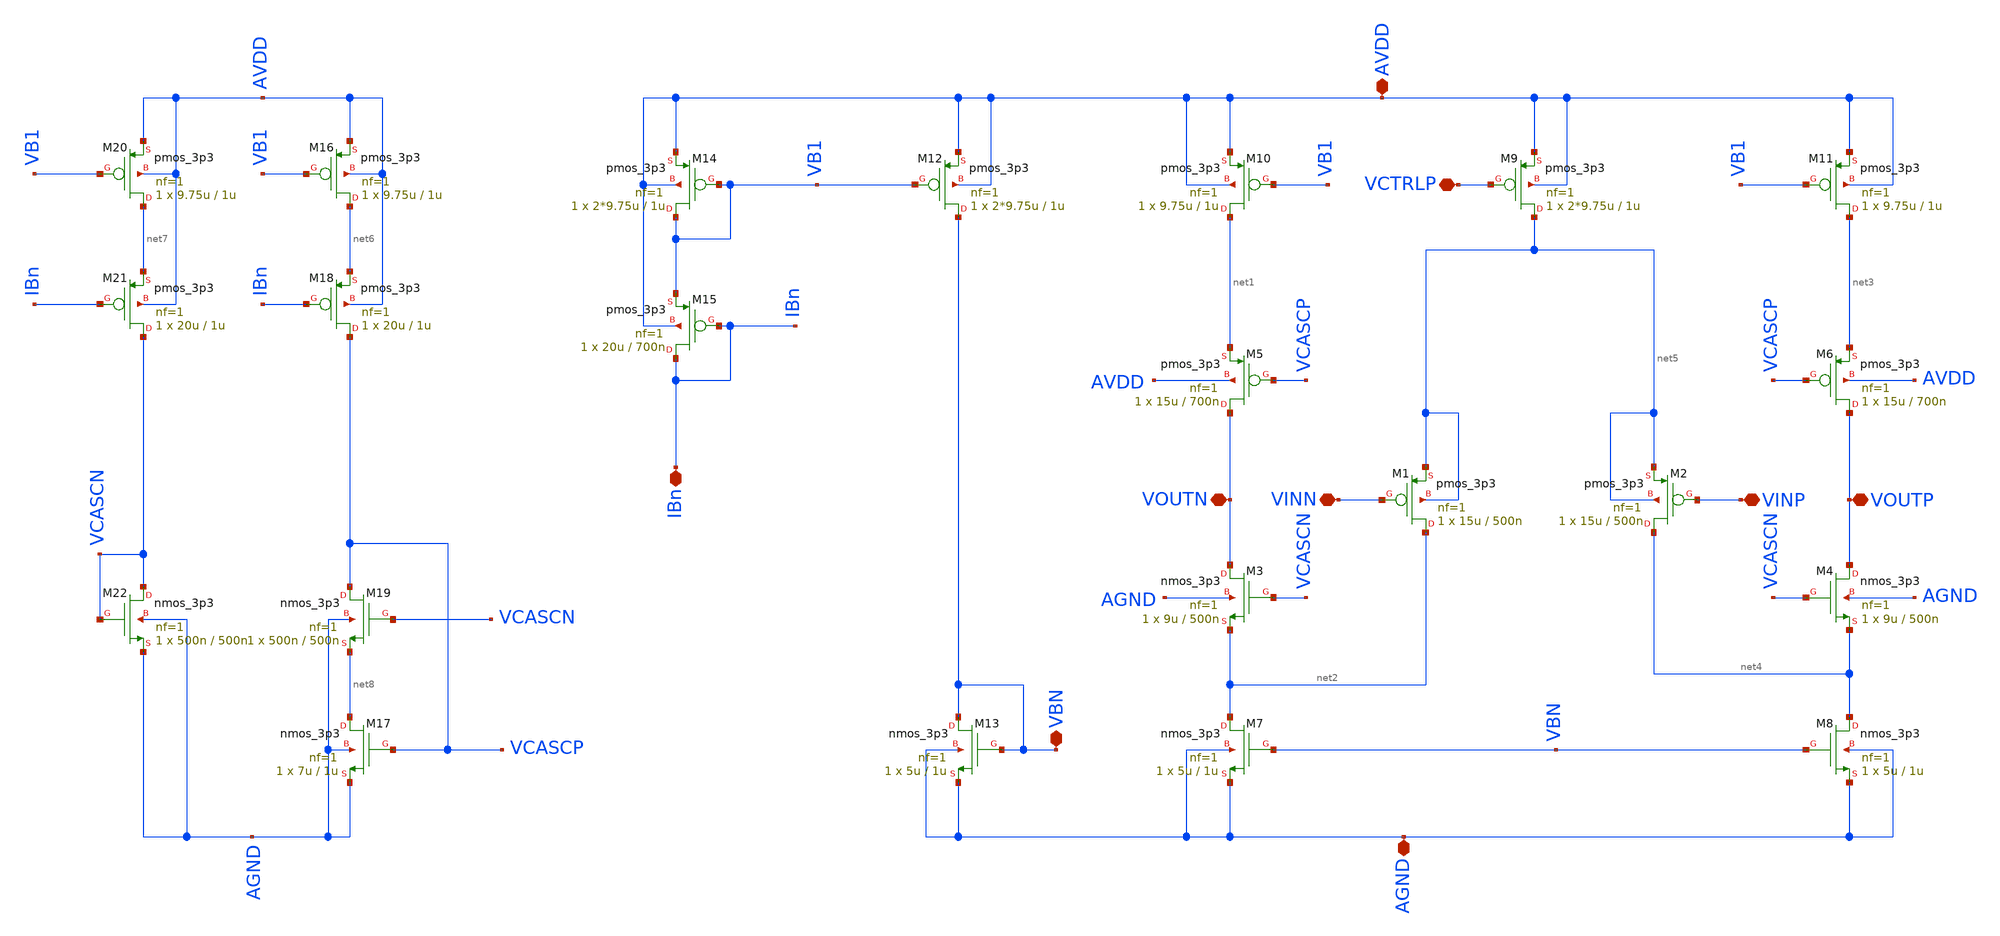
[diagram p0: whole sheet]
** sch_path: ITI_Labs/Lab11_Xschem/Design/OTA copy.sch
**.subckt OTA copy IBn AVDD AGND VINN VINP VOUTN VOUTP VCTRLP VBN
*.iopin IBn
*.iopin AVDD
*.iopin AGND
*.iopin VINN
*.iopin VINP
*.iopin VOUTN
*.iopin VOUTP
*.iopin VCTRLP
*.iopin VBN
XM2 net4 VINP net5 net5 pmos_3p3 L=500n W=15u nf=1 ad='int((nf+1)/2) * W/nf * 0.18u' as='int((nf+2)/2) * W/nf * 0.18u'
+ pd='2*int((nf+1)/2) * (W/nf + 0.18u)' ps='2*int((nf+2)/2) * (W/nf + 0.18u)' nrd='0.18u / W' nrs='0.18u / W'
+ sa=0 sb=0 sd=0 m=1
XM1 net2 VINN net5 net5 pmos_3p3 L=500n W=15u nf=1 ad='int((nf+1)/2) * W/nf * 0.18u' as='int((nf+2)/2) * W/nf * 0.18u'
+ pd='2*int((nf+1)/2) * (W/nf + 0.18u)' ps='2*int((nf+2)/2) * (W/nf + 0.18u)' nrd='0.18u / W' nrs='0.18u / W'
+ sa=0 sb=0 sd=0 m=1
XM9 net5 VCTRLP AVDD AVDD pmos_3p3 L=1u W=2*9.75u nf=1 ad='int((nf+1)/2) * W/nf * 0.18u' as='int((nf+2)/2) * W/nf * 0.18u'
+ pd='2*int((nf+1)/2) * (W/nf + 0.18u)' ps='2*int((nf+2)/2) * (W/nf + 0.18u)' nrd='0.18u / W' nrs='0.18u / W'
+ sa=0 sb=0 sd=0 m=1
XM6 VOUTP VCASCP net3 AVDD pmos_3p3 L=700n W=15u nf=1 ad='int((nf+1)/2) * W/nf * 0.18u' as='int((nf+2)/2) * W/nf * 0.18u'
+ pd='2*int((nf+1)/2) * (W/nf + 0.18u)' ps='2*int((nf+2)/2) * (W/nf + 0.18u)' nrd='0.18u / W' nrs='0.18u / W'
+ sa=0 sb=0 sd=0 m=1
XM11 net3 VB1 AVDD AVDD pmos_3p3 L=1u W=9.75u nf=1 ad='int((nf+1)/2) * W/nf * 0.18u' as='int((nf+2)/2) * W/nf * 0.18u'
+ pd='2*int((nf+1)/2) * (W/nf + 0.18u)' ps='2*int((nf+2)/2) * (W/nf + 0.18u)' nrd='0.18u / W' nrs='0.18u / W'
+ sa=0 sb=0 sd=0 m=1
XM4 VOUTP VCASCN net4 AGND nmos_3p3 L=500n W=9u nf=1 ad='int((nf+1)/2) * W/nf * 0.18u' as='int((nf+2)/2) * W/nf * 0.18u'
+ pd='2*int((nf+1)/2) * (W/nf + 0.18u)' ps='2*int((nf+2)/2) * (W/nf + 0.18u)' nrd='0.18u / W' nrs='0.18u / W'
+ sa=0 sb=0 sd=0 m=1
XM8 net4 VBN AGND AGND nmos_3p3 L=1u W=5u nf=1 ad='int((nf+1)/2) * W/nf * 0.18u' as='int((nf+2)/2) * W/nf * 0.18u'
+ pd='2*int((nf+1)/2) * (W/nf + 0.18u)' ps='2*int((nf+2)/2) * (W/nf + 0.18u)' nrd='0.18u / W' nrs='0.18u / W'
+ sa=0 sb=0 sd=0 m=1
XM5 VOUTN VCASCP net1 AVDD pmos_3p3 L=700n W=15u nf=1 ad='int((nf+1)/2) * W/nf * 0.18u' as='int((nf+2)/2) * W/nf * 0.18u'
+ pd='2*int((nf+1)/2) * (W/nf + 0.18u)' ps='2*int((nf+2)/2) * (W/nf + 0.18u)' nrd='0.18u / W' nrs='0.18u / W'
+ sa=0 sb=0 sd=0 m=1
XM10 net1 VB1 AVDD AVDD pmos_3p3 L=1u W=9.75u nf=1 ad='int((nf+1)/2) * W/nf * 0.18u' as='int((nf+2)/2) * W/nf * 0.18u'
+ pd='2*int((nf+1)/2) * (W/nf + 0.18u)' ps='2*int((nf+2)/2) * (W/nf + 0.18u)' nrd='0.18u / W' nrs='0.18u / W'
+ sa=0 sb=0 sd=0 m=1
XM3 VOUTN VCASCN net2 AGND nmos_3p3 L=500n W=9u nf=1 ad='int((nf+1)/2) * W/nf * 0.18u' as='int((nf+2)/2) * W/nf * 0.18u'
+ pd='2*int((nf+1)/2) * (W/nf + 0.18u)' ps='2*int((nf+2)/2) * (W/nf + 0.18u)' nrd='0.18u / W' nrs='0.18u / W'
+ sa=0 sb=0 sd=0 m=1
XM7 net2 VBN AGND AGND nmos_3p3 L=1u W=5u nf=1 ad='int((nf+1)/2) * W/nf * 0.18u' as='int((nf+2)/2) * W/nf * 0.18u'
+ pd='2*int((nf+1)/2) * (W/nf + 0.18u)' ps='2*int((nf+2)/2) * (W/nf + 0.18u)' nrd='0.18u / W' nrs='0.18u / W'
+ sa=0 sb=0 sd=0 m=1
XM12 VBN VB1 AVDD AVDD pmos_3p3 L=1u W=2*9.75u nf=1 ad='int((nf+1)/2) * W/nf * 0.18u' as='int((nf+2)/2) * W/nf * 0.18u'
+ pd='2*int((nf+1)/2) * (W/nf + 0.18u)' ps='2*int((nf+2)/2) * (W/nf + 0.18u)' nrd='0.18u / W' nrs='0.18u / W'
+ sa=0 sb=0 sd=0 m=1
XM13 VBN VBN AGND AGND nmos_3p3 L=1u W=5u nf=1 ad='int((nf+1)/2) * W/nf * 0.18u' as='int((nf+2)/2) * W/nf * 0.18u'
+ pd='2*int((nf+1)/2) * (W/nf + 0.18u)' ps='2*int((nf+2)/2) * (W/nf + 0.18u)' nrd='0.18u / W' nrs='0.18u / W'
+ sa=0 sb=0 sd=0 m=1
XM14 VB1 VB1 AVDD AVDD pmos_3p3 L=1u W=2*9.75u nf=1 ad='int((nf+1)/2) * W/nf * 0.18u' as='int((nf+2)/2) * W/nf * 0.18u'
+ pd='2*int((nf+1)/2) * (W/nf + 0.18u)' ps='2*int((nf+2)/2) * (W/nf + 0.18u)' nrd='0.18u / W' nrs='0.18u / W'
+ sa=0 sb=0 sd=0 m=1
XM15 IBn IBn VB1 AVDD pmos_3p3 L=700n W=20u nf=1 ad='int((nf+1)/2) * W/nf * 0.18u' as='int((nf+2)/2) * W/nf * 0.18u'
+ pd='2*int((nf+1)/2) * (W/nf + 0.18u)' ps='2*int((nf+2)/2) * (W/nf + 0.18u)' nrd='0.18u / W' nrs='0.18u / W'
+ sa=0 sb=0 sd=0 m=1
XM16 net6 VB1 AVDD AVDD pmos_3p3 L=1u W=9.75u nf=1 ad='int((nf+1)/2) * W/nf * 0.18u' as='int((nf+2)/2) * W/nf * 0.18u'
+ pd='2*int((nf+1)/2) * (W/nf + 0.18u)' ps='2*int((nf+2)/2) * (W/nf + 0.18u)' nrd='0.18u / W' nrs='0.18u / W'
+ sa=0 sb=0 sd=0 m=1
XM17 net8 VCASCP AGND AGND nmos_3p3 L=1u W=7u nf=1 ad='int((nf+1)/2) * W/nf * 0.18u' as='int((nf+2)/2) * W/nf * 0.18u'
+ pd='2*int((nf+1)/2) * (W/nf + 0.18u)' ps='2*int((nf+2)/2) * (W/nf + 0.18u)' nrd='0.18u / W' nrs='0.18u / W'
+ sa=0 sb=0 sd=0 m=1
XM18 VCASCP IBn net6 AVDD pmos_3p3 L=1u W=20u nf=1 ad='int((nf+1)/2) * W/nf * 0.18u' as='int((nf+2)/2) * W/nf * 0.18u'
+ pd='2*int((nf+1)/2) * (W/nf + 0.18u)' ps='2*int((nf+2)/2) * (W/nf + 0.18u)' nrd='0.18u / W' nrs='0.18u / W'
+ sa=0 sb=0 sd=0 m=1
XM19 VCASCP VCASCN net8 AGND nmos_3p3 L=500n W=500n nf=1 ad='int((nf+1)/2) * W/nf * 0.18u' as='int((nf+2)/2) * W/nf * 0.18u'
+ pd='2*int((nf+1)/2) * (W/nf + 0.18u)' ps='2*int((nf+2)/2) * (W/nf + 0.18u)' nrd='0.18u / W' nrs='0.18u / W'
+ sa=0 sb=0 sd=0 m=1
XM20 net7 VB1 AVDD AVDD pmos_3p3 L=1u W=9.75u nf=1 ad='int((nf+1)/2) * W/nf * 0.18u' as='int((nf+2)/2) * W/nf * 0.18u'
+ pd='2*int((nf+1)/2) * (W/nf + 0.18u)' ps='2*int((nf+2)/2) * (W/nf + 0.18u)' nrd='0.18u / W' nrs='0.18u / W'
+ sa=0 sb=0 sd=0 m=1
XM21 VCASCN IBn net7 AVDD pmos_3p3 L=1u W=20u nf=1 ad='int((nf+1)/2) * W/nf * 0.18u' as='int((nf+2)/2) * W/nf * 0.18u'
+ pd='2*int((nf+1)/2) * (W/nf + 0.18u)' ps='2*int((nf+2)/2) * (W/nf + 0.18u)' nrd='0.18u / W' nrs='0.18u / W'
+ sa=0 sb=0 sd=0 m=1
XM22 VCASCN VCASCN AGND AGND nmos_3p3 L=500n W=500n nf=1 ad='int((nf+1)/2) * W/nf * 0.18u' as='int((nf+2)/2) * W/nf * 0.18u'
+ pd='2*int((nf+1)/2) * (W/nf + 0.18u)' ps='2*int((nf+2)/2) * (W/nf + 0.18u)' nrd='0.18u / W' nrs='0.18u / W'
+ sa=0 sb=0 sd=0 m=1
**** begin user architecture code


**** end user architecture code
**.ends
.end
